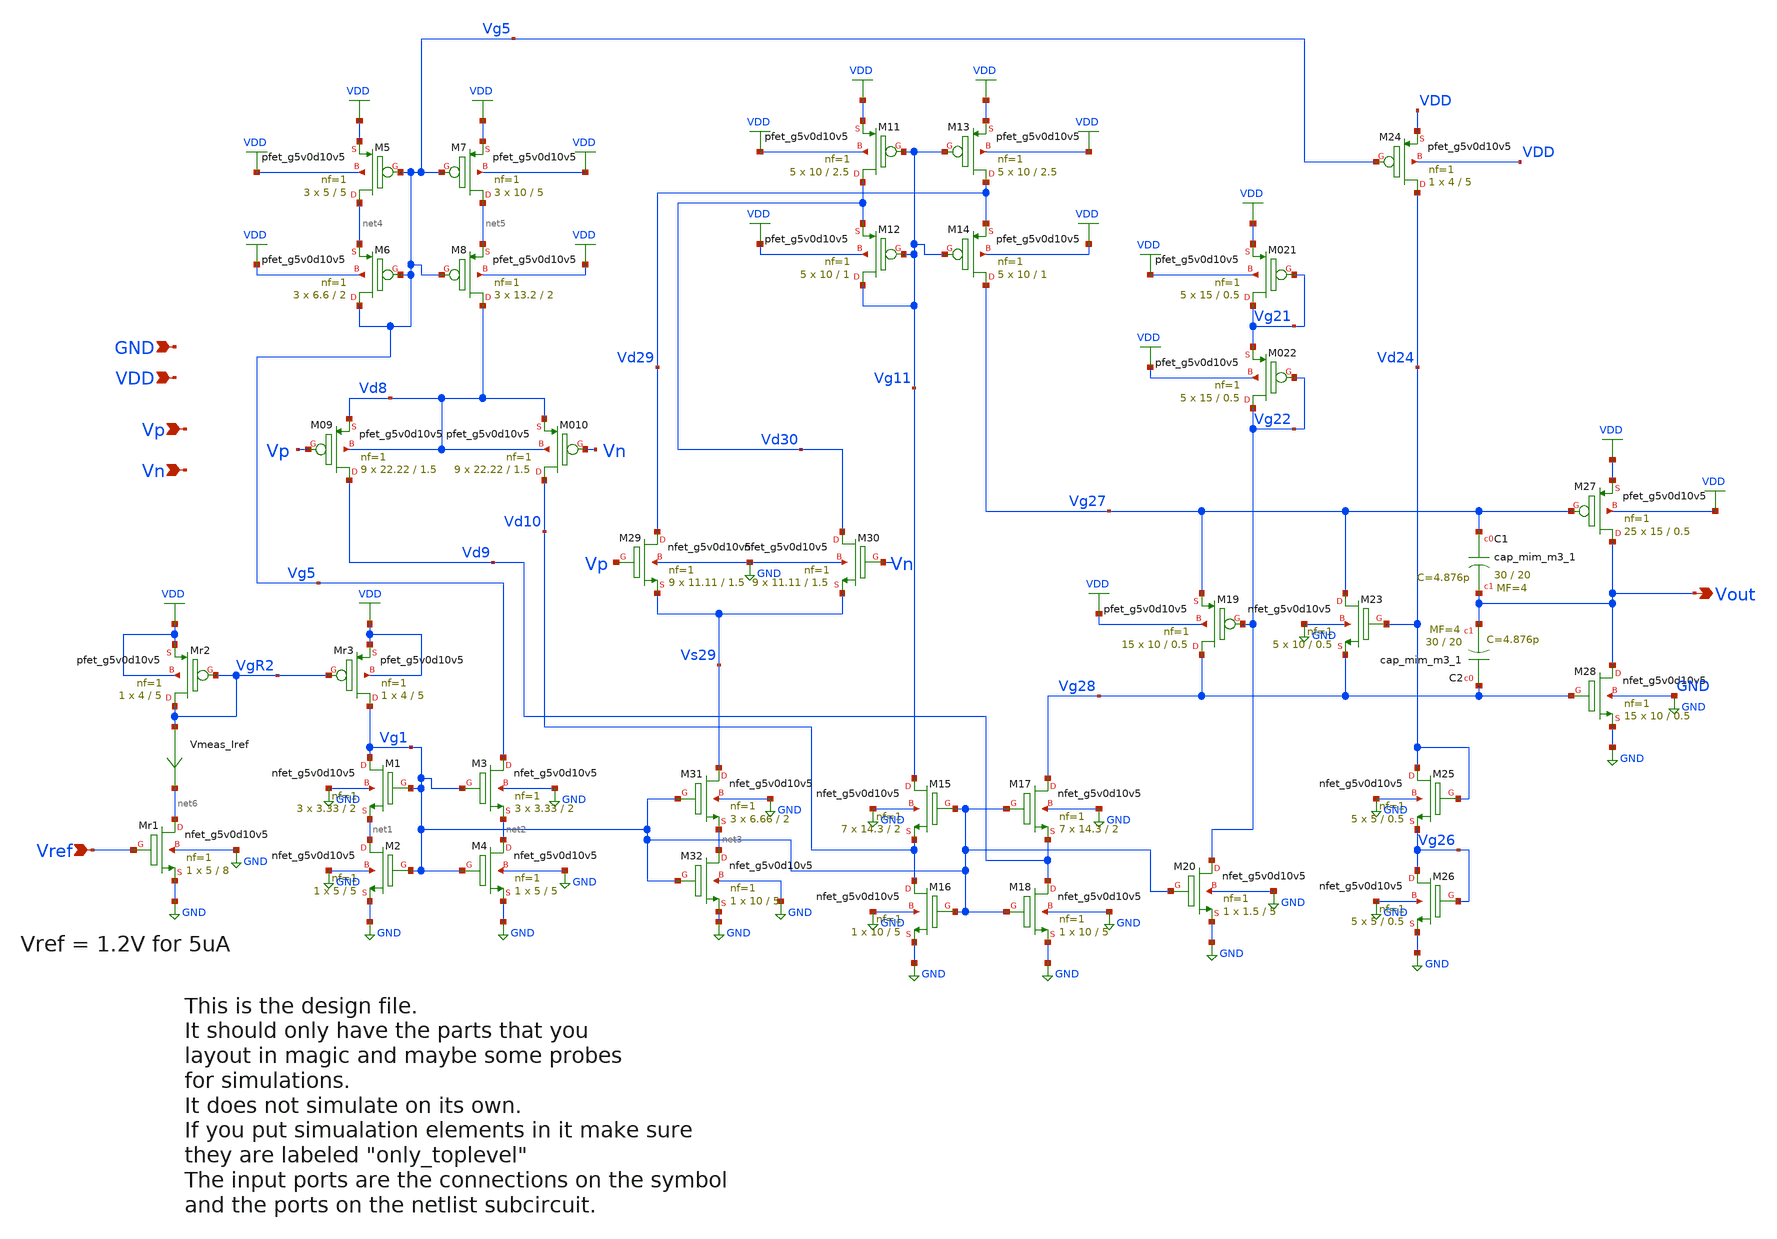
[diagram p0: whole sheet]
** sch_path: xschem/opamp.sch
* Copyright 2021 Stefan Frederik Schippers
* Licensed under the Apache License, Version 2.0 (the "License");
* you may not use this file except in compliance with the License.
* You may obtain a copy of the License at
* https://www.apache.org/licenses/LICENSE-2.0
* Unless required by applicable law or agreed to in writing, software
* distributed under the License is distributed on an "AS IS" BASIS,
* WITHOUT WARRANTIES OR CONDITIONS OF ANY KIND, either express or implied.
* See the License for the specific language governing permissions and
* limitations under the License.
**.subckt opamp Vout Vref Vp Vn GND VDD
*.opin Vout
*.ipin Vref
*.ipin Vp
*.ipin Vn
*.ipin GND
*.ipin VDD
XM1 Vg1 Vg1 net1 GND sky130_fd_pr__nfet_g5v0d10v5 L=2 W=3.33 nf=1 ad='int((1 + 1)/2) * 3.33 / 1 * 0.29'
+ as='int((1 + 2)/2) * 3.33 / 1 * 0.29' pd='2*int((1 + 1)/2) * (3.33 / 1 + 0.29)' ps='2*int((1 + 2)/2) * (3.33 / 1 + 0.29)'
+ nrd='0.29 / 3.33 ' nrs='0.29 / 3.33 ' sa=0 sb=0 sd=0 mult=3 m=3
XM2 net1 Vg1 GND GND sky130_fd_pr__nfet_g5v0d10v5 L=5 W=5 nf=1 ad='int((1 + 1)/2) * 5 / 1 * 0.29' as='int((1 + 2)/2) * 5 / 1 * 0.29'
+ pd='2*int((1 + 1)/2) * (5 / 1 + 0.29)' ps='2*int((1 + 2)/2) * (5 / 1 + 0.29)' nrd='0.29 / 5 ' nrs='0.29 / 5 '
+ sa=0 sb=0 sd=0 mult=1 m=1
XM4 net2 Vg1 GND GND sky130_fd_pr__nfet_g5v0d10v5 L=5 W=5 nf=1 ad='int((1 + 1)/2) * 5 / 1 * 0.29' as='int((1 + 2)/2) * 5 / 1 * 0.29'
+ pd='2*int((1 + 1)/2) * (5 / 1 + 0.29)' ps='2*int((1 + 2)/2) * (5 / 1 + 0.29)' nrd='0.29 / 5 ' nrs='0.29 / 5 '
+ sa=0 sb=0 sd=0 mult=1 m=1
XM3 Vg5 Vg1 net2 GND sky130_fd_pr__nfet_g5v0d10v5 L=2 W=3.33 nf=1 ad='int((1 + 1)/2) * 3.33 / 1 * 0.29'
+ as='int((1 + 2)/2) * 3.33 / 1 * 0.29' pd='2*int((1 + 1)/2) * (3.33 / 1 + 0.29)' ps='2*int((1 + 2)/2) * (3.33 / 1 + 0.29)'
+ nrd='0.29 / 3.33 ' nrs='0.29 / 3.33 ' sa=0 sb=0 sd=0 mult=3 m=3
XMr1 net6 Vref GND GND sky130_fd_pr__nfet_g5v0d10v5 L=8 W=5 nf=1 ad='int((1 + 1)/2) * 5 / 1 * 0.29' as='int((1 + 2)/2) * 5 / 1 * 0.29'
+ pd='2*int((1 + 1)/2) * (5 / 1 + 0.29)' ps='2*int((1 + 2)/2) * (5 / 1 + 0.29)' nrd='0.29 / 5 ' nrs='0.29 / 5 '
+ sa=0 sb=0 sd=0 mult=1 m=1
XMr2 VgR2 VgR2 VDD VDD sky130_fd_pr__pfet_g5v0d10v5 L=5 W=4 nf=1 ad='int((1 + 1)/2) * 4 / 1 * 0.29' as='int((1 + 2)/2) * 4 / 1 * 0.29'
+ pd='2*int((1 + 1)/2) * (4 / 1 + 0.29)' ps='2*int((1 + 2)/2) * (4 / 1 + 0.29)' nrd='0.29 / 4 ' nrs='0.29 / 4 '
+ sa=0 sb=0 sd=0 mult=1 m=1
XMr3 Vg1 VgR2 VDD VDD sky130_fd_pr__pfet_g5v0d10v5 L=5 W=4 nf=1 ad='int((1 + 1)/2) * 4 / 1 * 0.29' as='int((1 + 2)/2) * 4 / 1 * 0.29'
+ pd='2*int((1 + 1)/2) * (4 / 1 + 0.29)' ps='2*int((1 + 2)/2) * (4 / 1 + 0.29)' nrd='0.29 / 4 ' nrs='0.29 / 4 '
+ sa=0 sb=0 sd=0 mult=1 m=1
XM32 net3 Vg1 GND GND sky130_fd_pr__nfet_g5v0d10v5 L=5 W=10 nf=1 ad='int((1 + 1)/2) * 10 / 1 * 0.29'
+ as='int((1 + 2)/2) * 10 / 1 * 0.29' pd='2*int((1 + 1)/2) * (10 / 1 + 0.29)' ps='2*int((1 + 2)/2) * (10 / 1 + 0.29)'
+ nrd='0.29 / 10 ' nrs='0.29 / 10 ' sa=0 sb=0 sd=0 mult=1 m=1
XM31 Vs29 Vg1 net3 GND sky130_fd_pr__nfet_g5v0d10v5 L=2 W=6.66 nf=1 ad='int((1 + 1)/2) * 6.66 / 1 * 0.29'
+ as='int((1 + 2)/2) * 6.66 / 1 * 0.29' pd='2*int((1 + 1)/2) * (6.66 / 1 + 0.29)' ps='2*int((1 + 2)/2) * (6.66 / 1 + 0.29)'
+ nrd='0.29 / 6.66 ' nrs='0.29 / 6.66 ' sa=0 sb=0 sd=0 mult=3 m=3
XM15 Vg11 Vg1 Vd10 GND sky130_fd_pr__nfet_g5v0d10v5 L=2 W=14.3 nf=1 ad='int((1 + 1)/2) * 14.3 / 1 * 0.29'
+ as='int((1 + 2)/2) * 14.3 / 1 * 0.29' pd='2*int((1 + 1)/2) * (14.3 / 1 + 0.29)' ps='2*int((1 + 2)/2) * (14.3 / 1 + 0.29)'
+ nrd='0.29 / 14.3 ' nrs='0.29 / 14.3 ' sa=0 sb=0 sd=0 mult=7 m=7
XM16 Vd10 Vg1 GND GND sky130_fd_pr__nfet_g5v0d10v5 L=5 W=10 nf=1 ad='int((1 + 1)/2) * 10 / 1 * 0.29'
+ as='int((1 + 2)/2) * 10 / 1 * 0.29' pd='2*int((1 + 1)/2) * (10 / 1 + 0.29)' ps='2*int((1 + 2)/2) * (10 / 1 + 0.29)'
+ nrd='0.29 / 10 ' nrs='0.29 / 10 ' sa=0 sb=0 sd=0 mult=1 m=1
XM18 Vd9 Vg1 GND GND sky130_fd_pr__nfet_g5v0d10v5 L=5 W=10 nf=1 ad='int((1 + 1)/2) * 10 / 1 * 0.29' as='int((1 + 2)/2) * 10 / 1 * 0.29'
+ pd='2*int((1 + 1)/2) * (10 / 1 + 0.29)' ps='2*int((1 + 2)/2) * (10 / 1 + 0.29)' nrd='0.29 / 10 ' nrs='0.29 / 10 '
+ sa=0 sb=0 sd=0 mult=1 m=1
XM17 Vg28 Vg1 Vd9 GND sky130_fd_pr__nfet_g5v0d10v5 L=2 W=14.3 nf=1 ad='int((1 + 1)/2) * 14.3 / 1 * 0.29'
+ as='int((1 + 2)/2) * 14.3 / 1 * 0.29' pd='2*int((1 + 1)/2) * (14.3 / 1 + 0.29)' ps='2*int((1 + 2)/2) * (14.3 / 1 + 0.29)'
+ nrd='0.29 / 14.3 ' nrs='0.29 / 14.3 ' sa=0 sb=0 sd=0 mult=7 m=7
XM20 Vg22 Vg1 GND GND sky130_fd_pr__nfet_g5v0d10v5 L=5 W=1.5 nf=1 ad='int((1 + 1)/2) * 1.5 / 1 * 0.29'
+ as='int((1 + 2)/2) * 1.5 / 1 * 0.29' pd='2*int((1 + 1)/2) * (1.5 / 1 + 0.29)' ps='2*int((1 + 2)/2) * (1.5 / 1 + 0.29)'
+ nrd='0.29 / 1.5 ' nrs='0.29 / 1.5 ' sa=0 sb=0 sd=0 mult=1 m=1
XM26 Vg26 Vg26 GND GND sky130_fd_pr__nfet_g5v0d10v5 L=0.5 W=5 nf=1 ad='int((1 + 1)/2) * 5 / 1 * 0.29'
+ as='int((1 + 2)/2) * 5 / 1 * 0.29' pd='2*int((1 + 1)/2) * (5 / 1 + 0.29)' ps='2*int((1 + 2)/2) * (5 / 1 + 0.29)'
+ nrd='0.29 / 5 ' nrs='0.29 / 5 ' sa=0 sb=0 sd=0 mult=5 m=5
XM25 Vd24 Vd24 Vg26 GND sky130_fd_pr__nfet_g5v0d10v5 L=0.5 W=5 nf=1 ad='int((1 + 1)/2) * 5 / 1 * 0.29'
+ as='int((1 + 2)/2) * 5 / 1 * 0.29' pd='2*int((1 + 1)/2) * (5 / 1 + 0.29)' ps='2*int((1 + 2)/2) * (5 / 1 + 0.29)'
+ nrd='0.29 / 5 ' nrs='0.29 / 5 ' sa=0 sb=0 sd=0 mult=5 m=5
XM23 Vg27 Vd24 Vg28 GND sky130_fd_pr__nfet_g5v0d10v5 L=0.5 W=10 nf=1 ad='int((1 + 1)/2) * 10 / 1 * 0.29'
+ as='int((1 + 2)/2) * 10 / 1 * 0.29' pd='2*int((1 + 1)/2) * (10 / 1 + 0.29)' ps='2*int((1 + 2)/2) * (10 / 1 + 0.29)'
+ nrd='0.29 / 10 ' nrs='0.29 / 10 ' sa=0 sb=0 sd=0 mult=5 m=5
XM28 Vout Vg28 GND GND sky130_fd_pr__nfet_g5v0d10v5 L=0.5 W=10 nf=1 ad='int((1 + 1)/2) * 10 / 1 * 0.29'
+ as='int((1 + 2)/2) * 10 / 1 * 0.29' pd='2*int((1 + 1)/2) * (10 / 1 + 0.29)' ps='2*int((1 + 2)/2) * (10 / 1 + 0.29)'
+ nrd='0.29 / 10 ' nrs='0.29 / 10 ' sa=0 sb=0 sd=0 mult=15 m=15
XM30 Vd30 Vn Vs29 GND sky130_fd_pr__nfet_g5v0d10v5 L=1.5 W=11.11 nf=1 ad='int((1 + 1)/2) * 11.11 / 1 * 0.29'
+ as='int((1 + 2)/2) * 11.11 / 1 * 0.29' pd='2*int((1 + 1)/2) * (11.11 / 1 + 0.29)' ps='2*int((1 + 2)/2) * (11.11 / 1 + 0.29)'
+ nrd='0.29 / 11.11 ' nrs='0.29 / 11.11 ' sa=0 sb=0 sd=0 mult=9 m=9
XM29 Vd29 Vp Vs29 GND sky130_fd_pr__nfet_g5v0d10v5 L=1.5 W=11.11 nf=1 ad='int((1 + 1)/2) * 11.11 / 1 * 0.29'
+ as='int((1 + 2)/2) * 11.11 / 1 * 0.29' pd='2*int((1 + 1)/2) * (11.11 / 1 + 0.29)' ps='2*int((1 + 2)/2) * (11.11 / 1 + 0.29)'
+ nrd='0.29 / 11.11 ' nrs='0.29 / 11.11 ' sa=0 sb=0 sd=0 mult=9 m=9
XM5 net4 Vg5 VDD VDD sky130_fd_pr__pfet_g5v0d10v5 L=5 W=5 nf=1 ad='int((1 + 1)/2) * 5 / 1 * 0.29' as='int((1 + 2)/2) * 5 / 1 * 0.29'
+ pd='2*int((1 + 1)/2) * (5 / 1 + 0.29)' ps='2*int((1 + 2)/2) * (5 / 1 + 0.29)' nrd='0.29 / 5 ' nrs='0.29 / 5 '
+ sa=0 sb=0 sd=0 mult=3 m=3
XM6 Vg5 Vg5 net4 VDD sky130_fd_pr__pfet_g5v0d10v5 L=2 W=6.6 nf=1 ad='int((1 + 1)/2) * 6.6 / 1 * 0.29'
+ as='int((1 + 2)/2) * 6.6 / 1 * 0.29' pd='2*int((1 + 1)/2) * (6.6 / 1 + 0.29)' ps='2*int((1 + 2)/2) * (6.6 / 1 + 0.29)'
+ nrd='0.29 / 6.6 ' nrs='0.29 / 6.6 ' sa=0 sb=0 sd=0 mult=3 m=3
XM7 net5 Vg5 VDD VDD sky130_fd_pr__pfet_g5v0d10v5 L=5 W=10 nf=1 ad='int((1 + 1)/2) * 10 / 1 * 0.29' as='int((1 + 2)/2) * 10 / 1 * 0.29'
+ pd='2*int((1 + 1)/2) * (10 / 1 + 0.29)' ps='2*int((1 + 2)/2) * (10 / 1 + 0.29)' nrd='0.29 / 10 ' nrs='0.29 / 10 '
+ sa=0 sb=0 sd=0 mult=3 m=3
XM8 Vd8 Vg5 net5 VDD sky130_fd_pr__pfet_g5v0d10v5 L=2 W=13.2 nf=1 ad='int((1 + 1)/2) * 13.2 / 1 * 0.29'
+ as='int((1 + 2)/2) * 13.2 / 1 * 0.29' pd='2*int((1 + 1)/2) * (13.2 / 1 + 0.29)' ps='2*int((1 + 2)/2) * (13.2 / 1 + 0.29)'
+ nrd='0.29 / 13.2 ' nrs='0.29 / 13.2 ' sa=0 sb=0 sd=0 mult=3 m=3
XM09 Vd9 Vp Vd8 Vd8 sky130_fd_pr__pfet_g5v0d10v5 L=1.5 W=22.22 nf=1 ad='int((1 + 1)/2) * 22.22 / 1 * 0.29'
+ as='int((1 + 2)/2) * 22.22 / 1 * 0.29' pd='2*int((1 + 1)/2) * (22.22 / 1 + 0.29)' ps='2*int((1 + 2)/2) * (22.22 / 1 + 0.29)'
+ nrd='0.29 / 22.22 ' nrs='0.29 / 22.22 ' sa=0 sb=0 sd=0 mult=9 m=9
XM010 Vd10 Vn Vd8 Vd8 sky130_fd_pr__pfet_g5v0d10v5 L=1.5 W=22.22 nf=1 ad='int((1 + 1)/2) * 22.22 / 1 * 0.29'
+ as='int((1 + 2)/2) * 22.22 / 1 * 0.29' pd='2*int((1 + 1)/2) * (22.22 / 1 + 0.29)' ps='2*int((1 + 2)/2) * (22.22 / 1 + 0.29)'
+ nrd='0.29 / 22.22 ' nrs='0.29 / 22.22 ' sa=0 sb=0 sd=0 mult=9 m=9
XM13 Vd29 Vg11 VDD VDD sky130_fd_pr__pfet_g5v0d10v5 L=2.5 W=10 nf=1 ad='int((1 + 1)/2) * 10 / 1 * 0.29'
+ as='int((1 + 2)/2) * 10 / 1 * 0.29' pd='2*int((1 + 1)/2) * (10 / 1 + 0.29)' ps='2*int((1 + 2)/2) * (10 / 1 + 0.29)'
+ nrd='0.29 / 10 ' nrs='0.29 / 10 ' sa=0 sb=0 sd=0 mult=5 m=5
XM14 Vg27 Vg11 Vd29 VDD sky130_fd_pr__pfet_g5v0d10v5 L=1 W=10 nf=1 ad='int((1 + 1)/2) * 10 / 1 * 0.29'
+ as='int((1 + 2)/2) * 10 / 1 * 0.29' pd='2*int((1 + 1)/2) * (10 / 1 + 0.29)' ps='2*int((1 + 2)/2) * (10 / 1 + 0.29)'
+ nrd='0.29 / 10 ' nrs='0.29 / 10 ' sa=0 sb=0 sd=0 mult=5 m=5
XM11 Vd30 Vg11 VDD VDD sky130_fd_pr__pfet_g5v0d10v5 L=2.5 W=10 nf=1 ad='int((1 + 1)/2) * 10 / 1 * 0.29'
+ as='int((1 + 2)/2) * 10 / 1 * 0.29' pd='2*int((1 + 1)/2) * (10 / 1 + 0.29)' ps='2*int((1 + 2)/2) * (10 / 1 + 0.29)'
+ nrd='0.29 / 10 ' nrs='0.29 / 10 ' sa=0 sb=0 sd=0 mult=5 m=5
XM12 Vg11 Vg11 Vd30 VDD sky130_fd_pr__pfet_g5v0d10v5 L=1 W=10 nf=1 ad='int((1 + 1)/2) * 10 / 1 * 0.29'
+ as='int((1 + 2)/2) * 10 / 1 * 0.29' pd='2*int((1 + 1)/2) * (10 / 1 + 0.29)' ps='2*int((1 + 2)/2) * (10 / 1 + 0.29)'
+ nrd='0.29 / 10 ' nrs='0.29 / 10 ' sa=0 sb=0 sd=0 mult=5 m=5
XM021 Vg21 Vg21 VDD VDD sky130_fd_pr__pfet_g5v0d10v5 L=0.5 W=15 nf=1 ad='int((1 + 1)/2) * 15 / 1 * 0.29'
+ as='int((1 + 2)/2) * 15 / 1 * 0.29' pd='2*int((1 + 1)/2) * (15 / 1 + 0.29)' ps='2*int((1 + 2)/2) * (15 / 1 + 0.29)'
+ nrd='0.29 / 15 ' nrs='0.29 / 15 ' sa=0 sb=0 sd=0 mult=5 m=5
XM022 Vg22 Vg22 Vg21 VDD sky130_fd_pr__pfet_g5v0d10v5 L=0.5 W=15 nf=1 ad='int((1 + 1)/2) * 15 / 1 * 0.29'
+ as='int((1 + 2)/2) * 15 / 1 * 0.29' pd='2*int((1 + 1)/2) * (15 / 1 + 0.29)' ps='2*int((1 + 2)/2) * (15 / 1 + 0.29)'
+ nrd='0.29 / 15 ' nrs='0.29 / 15 ' sa=0 sb=0 sd=0 mult=5 m=5
XM24 Vd24 Vg5 VDD VDD sky130_fd_pr__pfet_g5v0d10v5 L=5 W=4 nf=1 ad='int((1 + 1)/2) * 4 / 1 * 0.29' as='int((1 + 2)/2) * 4 / 1 * 0.29'
+ pd='2*int((1 + 1)/2) * (4 / 1 + 0.29)' ps='2*int((1 + 2)/2) * (4 / 1 + 0.29)' nrd='0.29 / 4 ' nrs='0.29 / 4 '
+ sa=0 sb=0 sd=0 mult=1 m=1
XM27 Vout Vg27 VDD VDD sky130_fd_pr__pfet_g5v0d10v5 L=0.5 W=15 nf=1 ad='int((1 + 1)/2) * 15 / 1 * 0.29'
+ as='int((1 + 2)/2) * 15 / 1 * 0.29' pd='2*int((1 + 1)/2) * (15 / 1 + 0.29)' ps='2*int((1 + 2)/2) * (15 / 1 + 0.29)'
+ nrd='0.29 / 15 ' nrs='0.29 / 15 ' sa=0 sb=0 sd=0 mult=25 m=25
XM19 Vg28 Vg22 Vg27 VDD sky130_fd_pr__pfet_g5v0d10v5 L=0.5 W=10 nf=1 ad='int((1 + 1)/2) * 10 / 1 * 0.29'
+ as='int((1 + 2)/2) * 10 / 1 * 0.29' pd='2*int((1 + 1)/2) * (10 / 1 + 0.29)' ps='2*int((1 + 2)/2) * (10 / 1 + 0.29)'
+ nrd='0.29 / 10 ' nrs='0.29 / 10 ' sa=0 sb=0 sd=0 mult=15 m=15
Vmeas_Iref VgR2 net6 0
.save i(vmeas_iref)
XC1 Vg27 Vout sky130_fd_pr__cap_mim_m3_1 W=30 L=20 MF=4 m=4
XC2 Vg28 Vout sky130_fd_pr__cap_mim_m3_1 W=30 L=20 MF=4 m=4
**.ends
.GLOBAL VDD
.GLOBAL GND
.end
